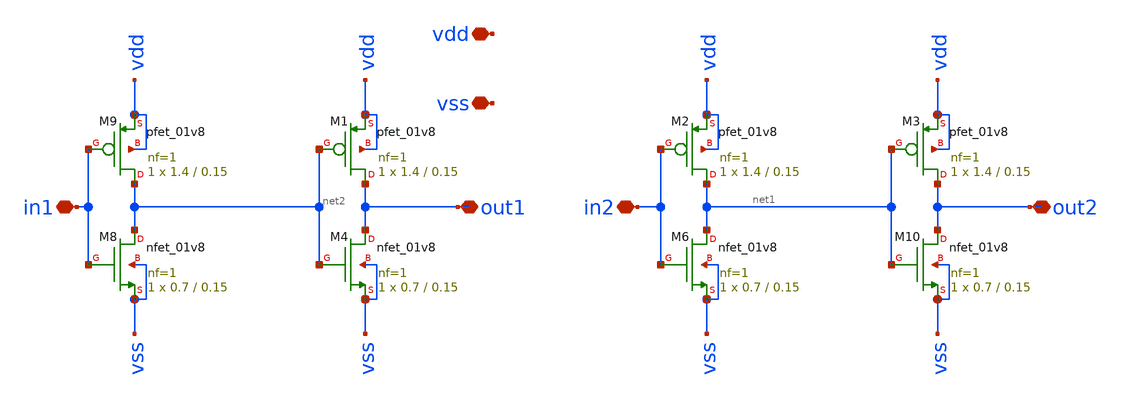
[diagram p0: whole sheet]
** sch_path: xschem/inv_buffer.sch
**.subckt inv_buffer in1 in2 out1 out2 vdd vss
*.iopin in1
*.iopin in2
*.iopin out1
*.iopin out2
*.iopin vdd
*.iopin vss
XM6 net1 in2 vss vss sky130_fd_pr__nfet_01v8 L=0.15 W=0.7 nf=1 ad='int((nf+1)/2) * W/nf * 0.29' as='int((nf+2)/2) * W/nf * 0.29'
+ pd='2*int((nf+1)/2) * (W/nf + 0.29)' ps='2*int((nf+2)/2) * (W/nf + 0.29)' nrd='0.29 / W' nrs='0.29 / W'
+ sa=0 sb=0 sd=0 mult=1 m=1
XM8 net2 in1 vss vss sky130_fd_pr__nfet_01v8 L=0.15 W=0.7 nf=1 ad='int((nf+1)/2) * W/nf * 0.29' as='int((nf+2)/2) * W/nf * 0.29'
+ pd='2*int((nf+1)/2) * (W/nf + 0.29)' ps='2*int((nf+2)/2) * (W/nf + 0.29)' nrd='0.29 / W' nrs='0.29 / W'
+ sa=0 sb=0 sd=0 mult=1 m=1
XM9 net2 in1 vdd vdd sky130_fd_pr__pfet_01v8 L=0.15 W=1.4 nf=1 ad='int((nf+1)/2) * W/nf * 0.29' as='int((nf+2)/2) * W/nf * 0.29'
+ pd='2*int((nf+1)/2) * (W/nf + 0.29)' ps='2*int((nf+2)/2) * (W/nf + 0.29)' nrd='0.29 / W' nrs='0.29 / W'
+ sa=0 sb=0 sd=0 mult=1 m=1
XM4 out1 net2 vss vss sky130_fd_pr__nfet_01v8 L=0.15 W=0.7 nf=1 ad='int((nf+1)/2) * W/nf * 0.29' as='int((nf+2)/2) * W/nf * 0.29'
+ pd='2*int((nf+1)/2) * (W/nf + 0.29)' ps='2*int((nf+2)/2) * (W/nf + 0.29)' nrd='0.29 / W' nrs='0.29 / W'
+ sa=0 sb=0 sd=0 mult=1 m=1
XM10 out2 net1 vss vss sky130_fd_pr__nfet_01v8 L=0.15 W=0.7 nf=1 ad='int((nf+1)/2) * W/nf * 0.29' as='int((nf+2)/2) * W/nf * 0.29'
+ pd='2*int((nf+1)/2) * (W/nf + 0.29)' ps='2*int((nf+2)/2) * (W/nf + 0.29)' nrd='0.29 / W' nrs='0.29 / W'
+ sa=0 sb=0 sd=0 mult=1 m=1
XM1 out1 net2 vdd vdd sky130_fd_pr__pfet_01v8 L=0.15 W=1.4 nf=1 ad='int((nf+1)/2) * W/nf * 0.29' as='int((nf+2)/2) * W/nf * 0.29'
+ pd='2*int((nf+1)/2) * (W/nf + 0.29)' ps='2*int((nf+2)/2) * (W/nf + 0.29)' nrd='0.29 / W' nrs='0.29 / W'
+ sa=0 sb=0 sd=0 mult=1 m=1
XM2 net1 in2 vdd vdd sky130_fd_pr__pfet_01v8 L=0.15 W=1.4 nf=1 ad='int((nf+1)/2) * W/nf * 0.29' as='int((nf+2)/2) * W/nf * 0.29'
+ pd='2*int((nf+1)/2) * (W/nf + 0.29)' ps='2*int((nf+2)/2) * (W/nf + 0.29)' nrd='0.29 / W' nrs='0.29 / W'
+ sa=0 sb=0 sd=0 mult=1 m=1
XM3 out2 net1 vdd vdd sky130_fd_pr__pfet_01v8 L=0.15 W=1.4 nf=1 ad='int((nf+1)/2) * W/nf * 0.29' as='int((nf+2)/2) * W/nf * 0.29'
+ pd='2*int((nf+1)/2) * (W/nf + 0.29)' ps='2*int((nf+2)/2) * (W/nf + 0.29)' nrd='0.29 / W' nrs='0.29 / W'
+ sa=0 sb=0 sd=0 mult=1 m=1
**.ends
.end
